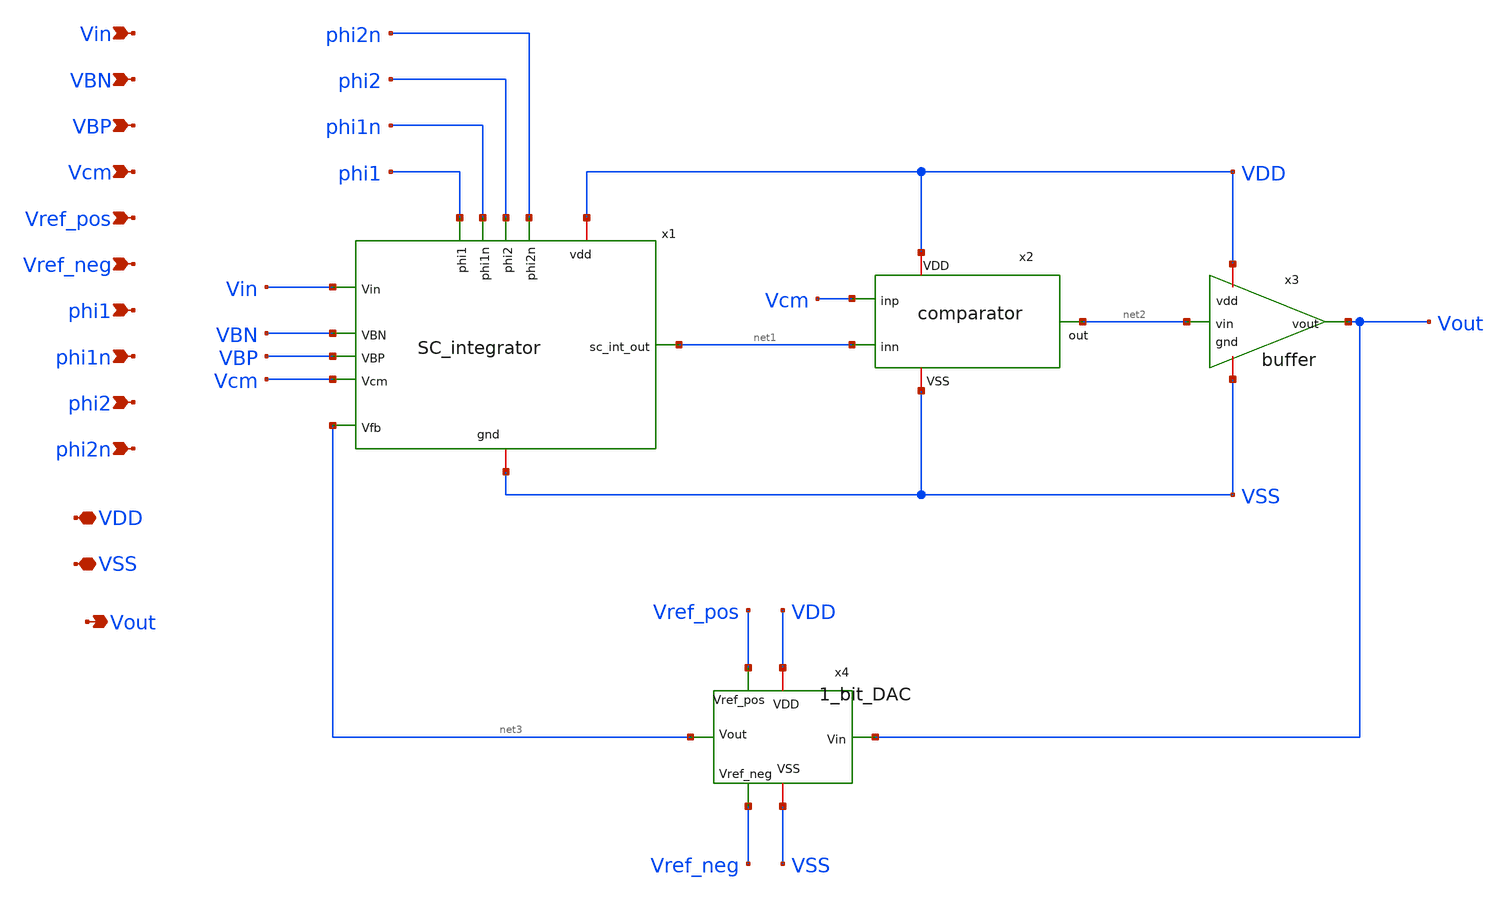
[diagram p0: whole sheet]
** sch_path: xschem/first_order_modulator.sch
**.subckt first_order_modulator Vin VBN VBP Vcm Vref_pos Vref_neg phi1 phi1n phi2 phi2n VDD VSS Vout
*.ipin Vin
*.ipin VBN
*.ipin VBP
*.ipin Vcm
*.ipin Vref_pos
*.ipin Vref_neg
*.ipin phi1
*.ipin phi1n
*.ipin phi2
*.ipin phi2n
*.iopin VDD
*.iopin VSS
*.opin Vout
x1 Vin net3 phi1 phi1n phi2 phi2n VBN VBP VDD VSS net1 Vcm SC_integrator
x2 VDD net2 net1 Vcm VSS comparator
x3 net2 VDD VSS Vout buffer
x4 Vout Vref_pos Vref_neg VDD net3 VSS 1_bit_DAC
**.ends
.end
